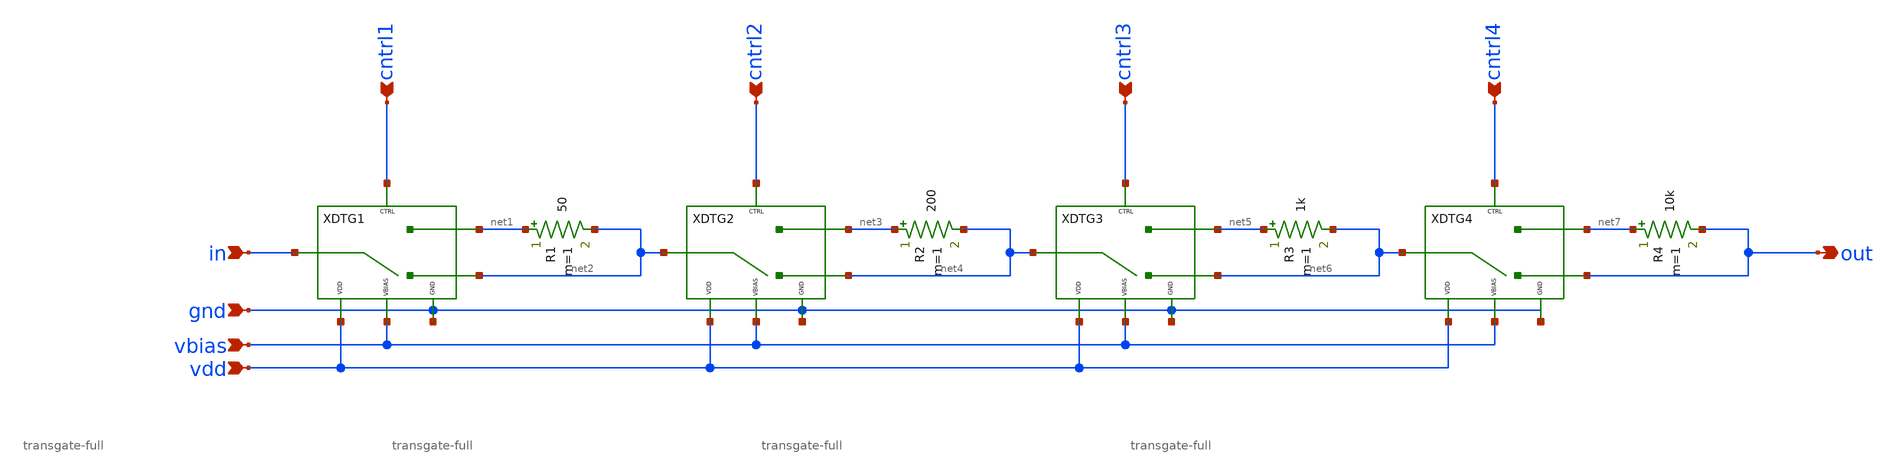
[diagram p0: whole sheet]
** sch_path: xschem/attenuator/dsa.sch
**.subckt dsa cntrl1 cntrl2 cntrl3 cntrl4 in out gnd vbias vdd
*.ipin cntrl1
*.ipin cntrl2
*.ipin cntrl3
*.ipin cntrl4
*.ipin in
*.opin out
*.ipin gnd
*.ipin vbias
*.ipin vdd
R1 net1 net2 50 m=1
R2 net3 net4 200 m=1
XDTG1 in cntrl1 vdd vbias gnd net2 net1 transgate-full
XDTG2 net2 cntrl2 vdd vbias gnd net4 net3 transgate-full
R3 net5 net6 1k m=1
XDTG3 net4 cntrl3 vdd vbias gnd net6 net5 transgate-full
R4 net7 out 10k m=1
XDTG4 net6 cntrl4 vdd vbias gnd out net7 transgate-full
**** begin user architecture code
 ** manual skywater pdks install (with patches applied)
* .lib $::SKYWATER_MODELS/models/sky130.lib.spice tt
*** remove the /models/

** opencircuitdesign pdks install
.lib /Volumes/WORK_DRIVE/open_pdks/sky130/custom/models/sky130.lib.spice tt

.param mc_mm_switch=0
.param mc_pr_switch=0

**** end user architecture code
**.ends
.end
